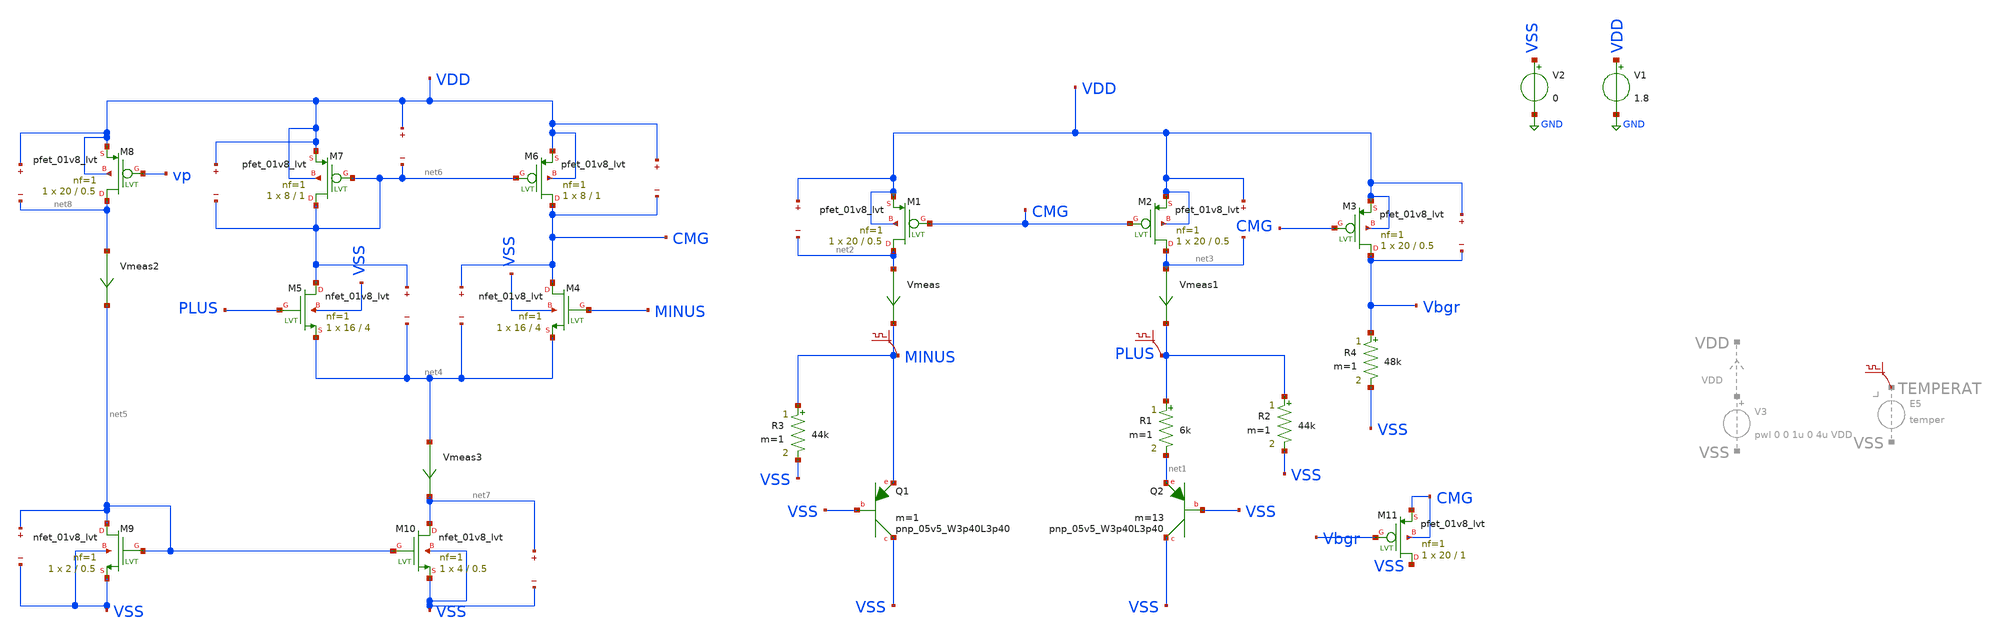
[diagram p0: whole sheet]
** sch_path: custom_gds/tt_um_bgr_agolmanesh/xschem/BGRwOpamp.sch
**.subckt BGRwOpamp
XQ1 VSS VSS MINUS sky130_fd_pr__pnp_05v5_W3p40L3p40 m=1
XQ2 VSS VSS net1 sky130_fd_pr__pnp_05v5_W3p40L3p40 m=13
XM1 net2 CMG VDD VDD sky130_fd_pr__pfet_01v8_lvt L=0.5 W=20 nf=1 ad='int((nf+1)/2) * W/nf * 0.29' as='int((nf+2)/2) * W/nf * 0.29'
+ pd='2*int((nf+1)/2) * (W/nf + 0.29)' ps='2*int((nf+2)/2) * (W/nf + 0.29)' nrd='0.29 / W' nrs='0.29 / W'
+ sa=0 sb=0 sd=0 mult=1 m=1
XM2 net3 CMG VDD VDD sky130_fd_pr__pfet_01v8_lvt L=0.5 W=20 nf=1 ad='int((nf+1)/2) * W/nf * 0.29' as='int((nf+2)/2) * W/nf * 0.29'
+ pd='2*int((nf+1)/2) * (W/nf + 0.29)' ps='2*int((nf+2)/2) * (W/nf + 0.29)' nrd='0.29 / W' nrs='0.29 / W'
+ sa=0 sb=0 sd=0 mult=1 m=1
XM3 Vbgr CMG VDD VDD sky130_fd_pr__pfet_01v8_lvt L=0.5 W=20 nf=1 ad='int((nf+1)/2) * W/nf * 0.29' as='int((nf+2)/2) * W/nf * 0.29'
+ pd='2*int((nf+1)/2) * (W/nf + 0.29)' ps='2*int((nf+2)/2) * (W/nf + 0.29)' nrd='0.29 / W' nrs='0.29 / W'
+ sa=0 sb=0 sd=0 mult=1 m=1
R1 PLUS net1 6k m=1
R2 PLUS VSS 44k m=1
R3 MINUS VSS 44k m=1
R4 Vbgr VSS 48k m=1
V1 VDD GND 1.8
V2 VSS GND 0
Vmeas net2 MINUS 0
.save i(vmeas)
Vmeas1 net3 PLUS 0
.save i(vmeas1)
.save v(vdd)
.save v(net2)
.save v(vdd)
.save v(net3)
.save v(vdd)
.save v(vbgr)
XM4 CMG MINUS net4 VSS sky130_fd_pr__nfet_01v8_lvt L=4 W=16 nf=1 ad='int((nf+1)/2) * W/nf * 0.29' as='int((nf+2)/2) * W/nf * 0.29'
+ pd='2*int((nf+1)/2) * (W/nf + 0.29)' ps='2*int((nf+2)/2) * (W/nf + 0.29)' nrd='0.29 / W' nrs='0.29 / W'
+ sa=0 sb=0 sd=0 mult=1 m=1
XM5 net6 PLUS net4 VSS sky130_fd_pr__nfet_01v8_lvt L=4 W=16 nf=1 ad='int((nf+1)/2) * W/nf * 0.29' as='int((nf+2)/2) * W/nf * 0.29'
+ pd='2*int((nf+1)/2) * (W/nf + 0.29)' ps='2*int((nf+2)/2) * (W/nf + 0.29)' nrd='0.29 / W' nrs='0.29 / W'
+ sa=0 sb=0 sd=0 mult=1 m=1
XM6 CMG net6 VDD VDD sky130_fd_pr__pfet_01v8_lvt L=1 W=8 nf=1 ad='int((nf+1)/2) * W/nf * 0.29' as='int((nf+2)/2) * W/nf * 0.29'
+ pd='2*int((nf+1)/2) * (W/nf + 0.29)' ps='2*int((nf+2)/2) * (W/nf + 0.29)' nrd='0.29 / W' nrs='0.29 / W'
+ sa=0 sb=0 sd=0 mult=1 m=1
.save v(cmg)
.save v(net4)
.save v(net6)
.save v(net4)
XM10 net7 net5 VSS VSS sky130_fd_pr__nfet_01v8_lvt L=0.5 W=4 nf=1 ad='int((nf+1)/2) * W/nf * 0.29' as='int((nf+2)/2) * W/nf * 0.29'
+ pd='2*int((nf+1)/2) * (W/nf + 0.29)' ps='2*int((nf+2)/2) * (W/nf + 0.29)' nrd='0.29 / W' nrs='0.29 / W'
+ sa=0 sb=0 sd=0 mult=1 m=1
XM9 net5 net5 VSS VSS sky130_fd_pr__nfet_01v8_lvt L=0.5 W=2 nf=1 ad='int((nf+1)/2) * W/nf * 0.29' as='int((nf+2)/2) * W/nf * 0.29'
+ pd='2*int((nf+1)/2) * (W/nf + 0.29)' ps='2*int((nf+2)/2) * (W/nf + 0.29)' nrd='0.29 / W' nrs='0.29 / W'
+ sa=0 sb=0 sd=0 mult=1 m=1
XM7 net6 net6 VDD VDD sky130_fd_pr__pfet_01v8_lvt L=1 W=8 nf=1 ad='int((nf+1)/2) * W/nf * 0.29' as='int((nf+2)/2) * W/nf * 0.29'
+ pd='2*int((nf+1)/2) * (W/nf + 0.29)' ps='2*int((nf+2)/2) * (W/nf + 0.29)' nrd='0.29 / W' nrs='0.29 / W'
+ sa=0 sb=0 sd=0 mult=1 m=1
.save v(vdd)
.save v(net6)
.save v(vdd)
.save v(cmg)
.save v(net7)
.save v(vss)
.save v(net5)
.save v(vss)
Vmeas3 net4 net7 0
.save i(vmeas3)
XM8 net8 vp VDD VDD sky130_fd_pr__pfet_01v8_lvt L=0.5 W=20 nf=1 ad='int((nf+1)/2) * W/nf * 0.29' as='int((nf+2)/2) * W/nf * 0.29'
+ pd='2*int((nf+1)/2) * (W/nf + 0.29)' ps='2*int((nf+2)/2) * (W/nf + 0.29)' nrd='0.29 / W' nrs='0.29 / W'
+ sa=0 sb=0 sd=0 mult=1 m=1
Vmeas2 net8 net5 0
.save i(vmeas2)
.save v(vdd)
.save v(net8)
.save v(vdd)
.save v(net6)
.save v(minus)
.save v(plus)
XM11 VSS Vbgr CMG CMG sky130_fd_pr__pfet_01v8_lvt L=1 W=20 nf=1 ad='int((nf+1)/2) * W/nf * 0.29' as='int((nf+2)/2) * W/nf * 0.29'
+ pd='2*int((nf+1)/2) * (W/nf + 0.29)' ps='2*int((nf+2)/2) * (W/nf + 0.29)' nrd='0.29 / W' nrs='0.29 / W'
+ sa=0 sb=0 sd=0 mult=1 m=1
**** begin user architecture code

** opencircuitdesign pdks install
.lib $::SKYWATER_MODELS/sky130.lib.spice tt


**** end user architecture code
**.ends
.GLOBAL GND
**** begin user architecture code



.options savecurrents
.control


save @m.xm1.msky130_fd_pr__ppet_01v8_lvt[gm]
save @m.xm1.msky130_fd_pr__pfet_01v8_lvt[id]
save @m.xm1.msky130_fd_pr__pfet_01v8_lvt[vgs]
save @m.xm1.msky130_fd_pr__pfet_01v8_lvt[vds]
save @m.xm1.msky130_fd_pr__pfet_01v8_lvt[cgg]
save @m.xm1.msky130_fd_pr__pfet_01v8_lvt[vdsat]
save @m.xm1.msky130_fd_pr__pfet_01v8_lvt[vth]


save @m.xm2.msky130_fd_pr__pfet_01v8_lvt[gm]
save @m.xm2.msky130_fd_pr__pfet_01v8_lvt[id]
save @m.xm2.msky130_fd_pr__pfet_01v8_lvt[vgs]
save @m.xm2.msky130_fd_pr__pfet_01v8_lvt[vds]
save @m.xm2.msky130_fd_pr__pfet_01v8_lvt[cgg]
save @m.xm2.msky130_fd_pr__pfet_01v8_lvt[vdsat]
save @m.xm2.msky130_fd_pr__pfet_01v8_lvt[vth]


save @m.xm3.msky130_fd_pr__pfet_01v8_lvt[gm]
save @m.xm3.msky130_fd_pr__pfet_01v8_lvt[id]
save @m.xm3.msky130_fd_pr__pfet_01v8_lvt[vgs]
save @m.xm3.msky130_fd_pr__pfet_01v8_lvt[vds]
save @m.xm3.msky130_fd_pr__pfet_01v8_lvt[cgg]
save @m.xm3.msky130_fd_pr__pfet_01v8_lvt[vdsat]
save @m.xm3.msky130_fd_pr__pfet_01v8_lvt[vth]

save @q.xq1.qsky130_fd_pr__pnp_05v5_W3p40L3p40[vbe]
save @q.xq2.qsky130_fd_pr__pnp_05v5_W3p40L3p40[vbe]


save @m.xm6.msky130_fd_pr__pfet_01v8_lvt[gm]
save @m.xm6.msky130_fd_pr__pfet_01v8_lvt[id]
save @m.xm6.msky130_fd_pr__pfet_01v8_lvt[vgs]
save @m.xm6.msky130_fd_pr__pfet_01v8_lvt[vds]
save @m.xm6.msky130_fd_pr__pfet_01v8_lvt[cgg]
save @m.xm6.msky130_fd_pr__pfet_01v8_lvt[vdsat]
save @m.xm6.msky130_fd_pr__pfet_01v8_lvt[vth]

save @m.xm7.msky130_fd_pr__pfet_01v8_lvt[gm]
save @m.xm7.msky130_fd_pr__pfet_01v8_lvt[id]
save @m.xm7.msky130_fd_pr__pfet_01v8_lvt[vgs]
save @m.xm7.msky130_fd_pr__pfet_01v8_lvt[vds]
save @m.xm7.msky130_fd_pr__pfet_01v8_lvt[cgg]
save @m.xm7.msky130_fd_pr__pfet_01v8_lvt[vdsat]
save @m.xm7.msky130_fd_pr__pfet_01v8_lvt[vth]



save @m.xm8.msky130_fd_pr__pfet_01v8_lvt[gm]
save @m.xm8.msky130_fd_pr__pfet_01v8_lvt[id]
save @m.xm8.msky130_fd_pr__pfet_01v8_lvt[vgs]
save @m.xm8.msky130_fd_pr__pfet_01v8_lvt[vds]
save @m.xm8.msky130_fd_pr__pfet_01v8_lvt[cgg]
save @m.xm8.msky130_fd_pr__pfet_01v8_lvt[vdsat]
save @m.xm8.msky130_fd_pr__pfet_01v8_lvt[vth]


save @m.xm4.msky130_fd_pr__nfet_01v8_lvt[gm]
save @m.xm4.msky130_fd_pr__nfet_01v8_lvt[id]
save @m.xm4.msky130_fd_pr__nfet_01v8_lvt[vgs]
save @m.xm4.msky130_fd_pr__nfet_01v8_lvt[vds]
save @m.xm4.msky130_fd_pr__nfet_01v8_lvt[cgg]
save @m.xm4.msky130_fd_pr__nfet_01v8_lvt[vdsat]
save @m.xm4.msky130_fd_pr__nfet_01v8_lvt[vth]


save @m.xm5.msky130_fd_pr__nfet_01v8_lvt[gm]
save @m.xm5.msky130_fd_pr__nfet_01v8_lvt[id]
save @m.xm5.msky130_fd_pr__nfet_01v8_lvt[vgs]
save @m.xm5.msky130_fd_pr__nfet_01v8_lvt[vds]
save @m.xm5.msky130_fd_pr__nfet_01v8_lvt[cgg]
save @m.xm5.msky130_fd_pr__nfet_01v8_lvt[vdsat]
save @m.xm5.msky130_fd_pr__nfet_01v8_lvt[vth]



save @m.xm9.msky130_fd_pr__nfet_01v8_lvt[gm]
save @m.xm9.msky130_fd_pr__nfet_01v8_lvt[id]
save @m.xm9.msky130_fd_pr__nfet_01v8_lvt[vgs]
save @m.xm9.msky130_fd_pr__nfet_01v8_lvt[vds]
save @m.xm9.msky130_fd_pr__nfet_01v8_lvt[cgg]
save @m.xm9.msky130_fd_pr__nfet_01v8_lvt[vdsat]
save @m.xm9.msky130_fd_pr__nfet_01v8_lvt[vth]



save @m.xm10.msky130_fd_pr__nfet_01v8_lvt[gm]
save @m.xm10.msky130_fd_pr__nfet_01v8_lvt[id]
save @m.xm10.msky130_fd_pr__nfet_01v8_lvt[vgs]
save @m.xm10.msky130_fd_pr__nfet_01v8_lvt[vds]
save @m.xm10.msky130_fd_pr__nfet_01v8_lvt[cgg]
save @m.xm10.msky130_fd_pr__nfet_01v8_lvt[vdsat]
save @m.xm10.msky130_fd_pr__nfet_01v8_lvt[vth]

save all
op
write BGRwOpamp.raw
dc TEMP -40 125 10
plot deriv(Vbgr)
.endc



**** end user architecture code
.end
